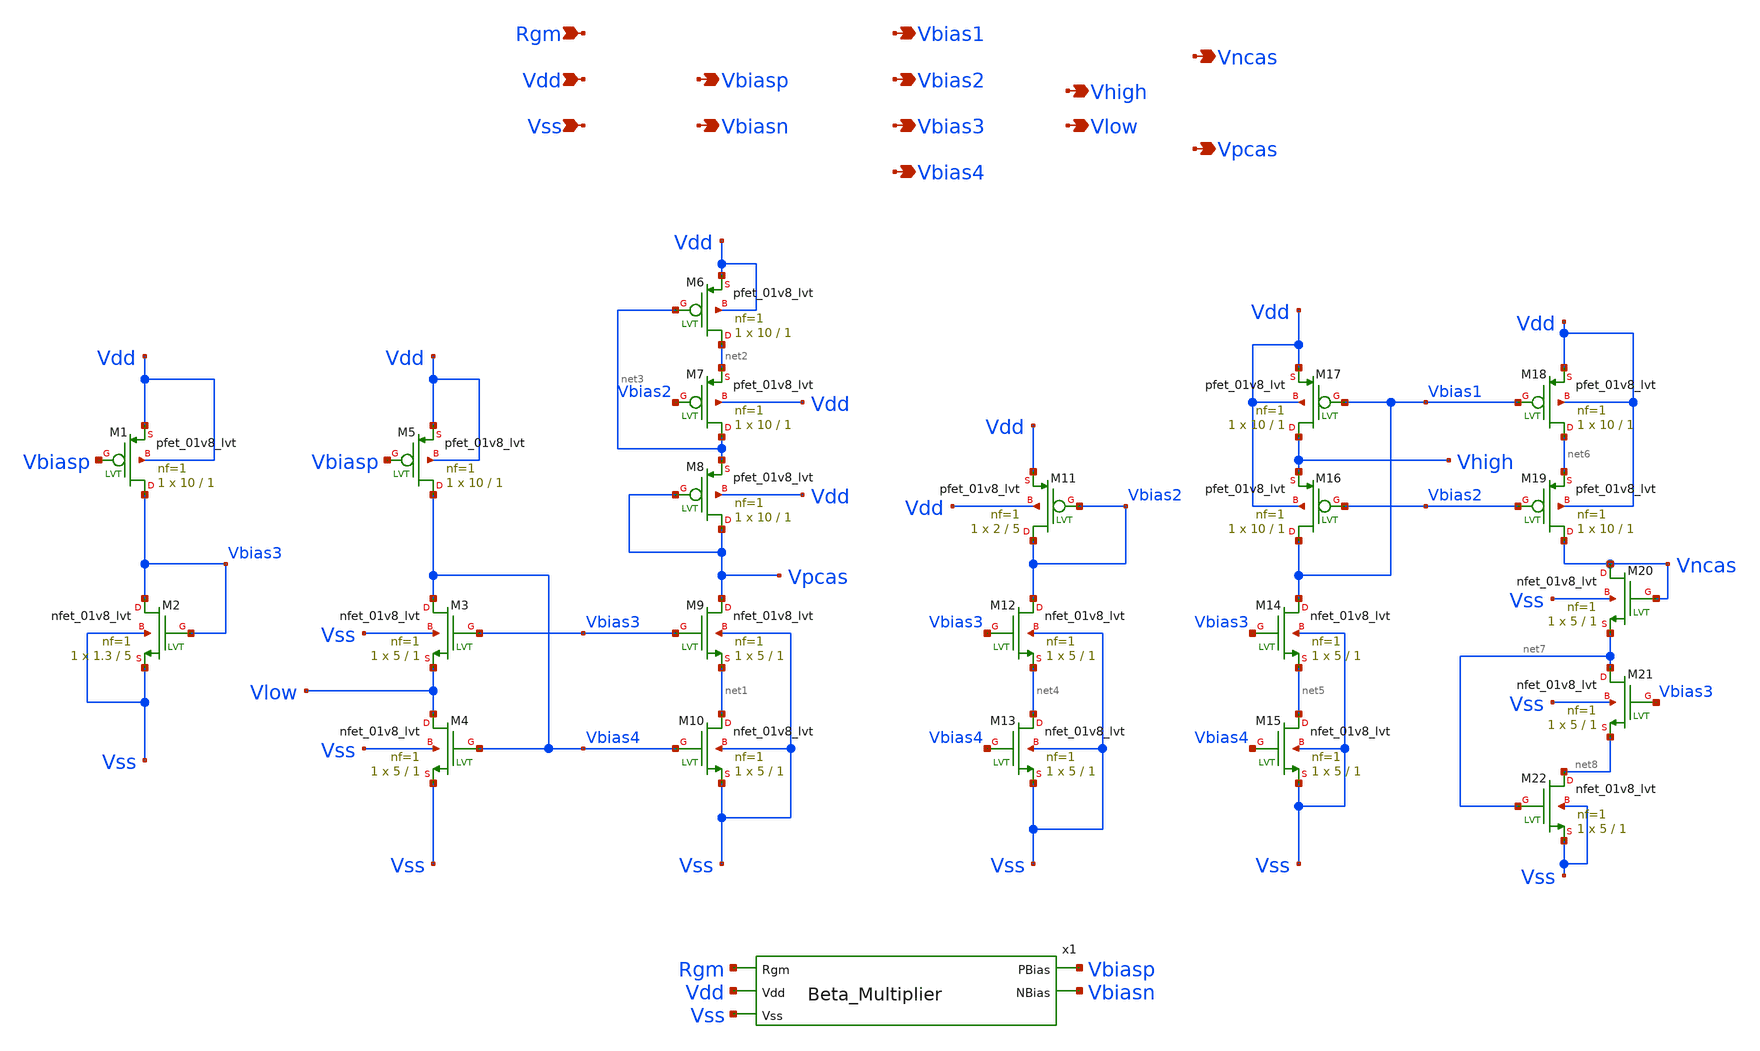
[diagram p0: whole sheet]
** sch_path: src/Opamp_Design/src/Bias_Circuit.sch
**.subckt Bias_Circuit Vdd Vbiasp Vss Vbiasn Vbias1 Vbias2 Vbias3 Vbias4 Vpcas Vlow Vncas Vhigh Rgm
*.ipin Vdd
*.opin Vbiasp
*.ipin Vss
*.opin Vbiasn
*.opin Vbias1
*.opin Vbias2
*.opin Vbias3
*.opin Vbias4
*.opin Vpcas
*.opin Vlow
*.opin Vncas
*.opin Vhigh
*.ipin Rgm
XM1 Vbias3 Vbiasp Vdd Vdd sky130_fd_pr__pfet_01v8_lvt L=1 W=10 nf=1 ad='int((nf+1)/2) * W/nf * 0.29'
+ as='int((nf+2)/2) * W/nf * 0.29' pd='2*int((nf+1)/2) * (W/nf + 0.29)' ps='2*int((nf+2)/2) * (W/nf + 0.29)'
+ nrd='0.29 / W' nrs='0.29 / W' sa=0 sb=0 sd=0 mult=1 m=1
XM2 Vbias3 Vbias3 Vss Vss sky130_fd_pr__nfet_01v8_lvt L=5 W=1.3 nf=1 ad='int((nf+1)/2) * W/nf * 0.29'
+ as='int((nf+2)/2) * W/nf * 0.29' pd='2*int((nf+1)/2) * (W/nf + 0.29)' ps='2*int((nf+2)/2) * (W/nf + 0.29)'
+ nrd='0.29 / W' nrs='0.29 / W' sa=0 sb=0 sd=0 mult=1 m=1
XM3 Vbias4 Vbias3 Vlow Vss sky130_fd_pr__nfet_01v8_lvt L=1 W=5 nf=1 ad='int((nf+1)/2) * W/nf * 0.29'
+ as='int((nf+2)/2) * W/nf * 0.29' pd='2*int((nf+1)/2) * (W/nf + 0.29)' ps='2*int((nf+2)/2) * (W/nf + 0.29)'
+ nrd='0.29 / W' nrs='0.29 / W' sa=0 sb=0 sd=0 mult=1 m=1
XM4 Vlow Vbias4 Vss Vss sky130_fd_pr__nfet_01v8_lvt L=1 W=5 nf=1 ad='int((nf+1)/2) * W/nf * 0.29' as='int((nf+2)/2) * W/nf * 0.29'
+ pd='2*int((nf+1)/2) * (W/nf + 0.29)' ps='2*int((nf+2)/2) * (W/nf + 0.29)' nrd='0.29 / W' nrs='0.29 / W'
+ sa=0 sb=0 sd=0 mult=1 m=1
XM5 Vbias4 Vbiasp Vdd Vdd sky130_fd_pr__pfet_01v8_lvt L=1 W=10 nf=1 ad='int((nf+1)/2) * W/nf * 0.29'
+ as='int((nf+2)/2) * W/nf * 0.29' pd='2*int((nf+1)/2) * (W/nf + 0.29)' ps='2*int((nf+2)/2) * (W/nf + 0.29)'
+ nrd='0.29 / W' nrs='0.29 / W' sa=0 sb=0 sd=0 mult=1 m=1
XM6 net2 net3 Vdd Vdd sky130_fd_pr__pfet_01v8_lvt L=1 W=10 nf=1 ad='int((nf+1)/2) * W/nf * 0.29' as='int((nf+2)/2) * W/nf * 0.29'
+ pd='2*int((nf+1)/2) * (W/nf + 0.29)' ps='2*int((nf+2)/2) * (W/nf + 0.29)' nrd='0.29 / W' nrs='0.29 / W'
+ sa=0 sb=0 sd=0 mult=1 m=1
XM7 net3 Vbias2 net2 Vdd sky130_fd_pr__pfet_01v8_lvt L=1 W=10 nf=1 ad='int((nf+1)/2) * W/nf * 0.29' as='int((nf+2)/2) * W/nf * 0.29'
+ pd='2*int((nf+1)/2) * (W/nf + 0.29)' ps='2*int((nf+2)/2) * (W/nf + 0.29)' nrd='0.29 / W' nrs='0.29 / W'
+ sa=0 sb=0 sd=0 mult=1 m=1
XM8 Vpcas Vpcas net3 Vdd sky130_fd_pr__pfet_01v8_lvt L=1 W=10 nf=1 ad='int((nf+1)/2) * W/nf * 0.29' as='int((nf+2)/2) * W/nf * 0.29'
+ pd='2*int((nf+1)/2) * (W/nf + 0.29)' ps='2*int((nf+2)/2) * (W/nf + 0.29)' nrd='0.29 / W' nrs='0.29 / W'
+ sa=0 sb=0 sd=0 mult=1 m=1
XM9 Vpcas Vbias3 net1 Vss sky130_fd_pr__nfet_01v8_lvt L=1 W=5 nf=1 ad='int((nf+1)/2) * W/nf * 0.29' as='int((nf+2)/2) * W/nf * 0.29'
+ pd='2*int((nf+1)/2) * (W/nf + 0.29)' ps='2*int((nf+2)/2) * (W/nf + 0.29)' nrd='0.29 / W' nrs='0.29 / W'
+ sa=0 sb=0 sd=0 mult=1 m=1
XM10 net1 Vbias4 Vss Vss sky130_fd_pr__nfet_01v8_lvt L=1 W=5 nf=1 ad='int((nf+1)/2) * W/nf * 0.29' as='int((nf+2)/2) * W/nf * 0.29'
+ pd='2*int((nf+1)/2) * (W/nf + 0.29)' ps='2*int((nf+2)/2) * (W/nf + 0.29)' nrd='0.29 / W' nrs='0.29 / W'
+ sa=0 sb=0 sd=0 mult=1 m=1
XM11 Vbias2 Vbias2 Vdd Vdd sky130_fd_pr__pfet_01v8_lvt L=5 W=2 nf=1 ad='int((nf+1)/2) * W/nf * 0.29'
+ as='int((nf+2)/2) * W/nf * 0.29' pd='2*int((nf+1)/2) * (W/nf + 0.29)' ps='2*int((nf+2)/2) * (W/nf + 0.29)'
+ nrd='0.29 / W' nrs='0.29 / W' sa=0 sb=0 sd=0 mult=1 m=1
XM12 Vbias2 Vbias3 net4 Vss sky130_fd_pr__nfet_01v8_lvt L=1 W=5 nf=1 ad='int((nf+1)/2) * W/nf * 0.29'
+ as='int((nf+2)/2) * W/nf * 0.29' pd='2*int((nf+1)/2) * (W/nf + 0.29)' ps='2*int((nf+2)/2) * (W/nf + 0.29)'
+ nrd='0.29 / W' nrs='0.29 / W' sa=0 sb=0 sd=0 mult=1 m=1
XM13 net4 Vbias4 Vss Vss sky130_fd_pr__nfet_01v8_lvt L=1 W=5 nf=1 ad='int((nf+1)/2) * W/nf * 0.29' as='int((nf+2)/2) * W/nf * 0.29'
+ pd='2*int((nf+1)/2) * (W/nf + 0.29)' ps='2*int((nf+2)/2) * (W/nf + 0.29)' nrd='0.29 / W' nrs='0.29 / W'
+ sa=0 sb=0 sd=0 mult=1 m=1
XM14 Vbias1 Vbias3 net5 Vss sky130_fd_pr__nfet_01v8_lvt L=1 W=5 nf=1 ad='int((nf+1)/2) * W/nf * 0.29'
+ as='int((nf+2)/2) * W/nf * 0.29' pd='2*int((nf+1)/2) * (W/nf + 0.29)' ps='2*int((nf+2)/2) * (W/nf + 0.29)'
+ nrd='0.29 / W' nrs='0.29 / W' sa=0 sb=0 sd=0 mult=1 m=1
XM15 net5 Vbias4 Vss Vss sky130_fd_pr__nfet_01v8_lvt L=1 W=5 nf=1 ad='int((nf+1)/2) * W/nf * 0.29' as='int((nf+2)/2) * W/nf * 0.29'
+ pd='2*int((nf+1)/2) * (W/nf + 0.29)' ps='2*int((nf+2)/2) * (W/nf + 0.29)' nrd='0.29 / W' nrs='0.29 / W'
+ sa=0 sb=0 sd=0 mult=1 m=1
XM16 Vbias1 Vbias2 Vhigh Vdd sky130_fd_pr__pfet_01v8_lvt L=1 W=10 nf=1 ad='int((nf+1)/2) * W/nf * 0.29'
+ as='int((nf+2)/2) * W/nf * 0.29' pd='2*int((nf+1)/2) * (W/nf + 0.29)' ps='2*int((nf+2)/2) * (W/nf + 0.29)'
+ nrd='0.29 / W' nrs='0.29 / W' sa=0 sb=0 sd=0 mult=1 m=1
XM17 Vhigh Vbias1 Vdd Vdd sky130_fd_pr__pfet_01v8_lvt L=1 W=10 nf=1 ad='int((nf+1)/2) * W/nf * 0.29'
+ as='int((nf+2)/2) * W/nf * 0.29' pd='2*int((nf+1)/2) * (W/nf + 0.29)' ps='2*int((nf+2)/2) * (W/nf + 0.29)'
+ nrd='0.29 / W' nrs='0.29 / W' sa=0 sb=0 sd=0 mult=1 m=1
XM18 net6 Vbias1 Vdd Vdd sky130_fd_pr__pfet_01v8_lvt L=1 W=10 nf=1 ad='int((nf+1)/2) * W/nf * 0.29' as='int((nf+2)/2) * W/nf * 0.29'
+ pd='2*int((nf+1)/2) * (W/nf + 0.29)' ps='2*int((nf+2)/2) * (W/nf + 0.29)' nrd='0.29 / W' nrs='0.29 / W'
+ sa=0 sb=0 sd=0 mult=1 m=1
XM19 Vncas Vbias2 net6 Vdd sky130_fd_pr__pfet_01v8_lvt L=1 W=10 nf=1 ad='int((nf+1)/2) * W/nf * 0.29'
+ as='int((nf+2)/2) * W/nf * 0.29' pd='2*int((nf+1)/2) * (W/nf + 0.29)' ps='2*int((nf+2)/2) * (W/nf + 0.29)'
+ nrd='0.29 / W' nrs='0.29 / W' sa=0 sb=0 sd=0 mult=1 m=1
XM20 Vncas Vncas net7 Vss sky130_fd_pr__nfet_01v8_lvt L=1 W=5 nf=1 ad='int((nf+1)/2) * W/nf * 0.29' as='int((nf+2)/2) * W/nf * 0.29'
+ pd='2*int((nf+1)/2) * (W/nf + 0.29)' ps='2*int((nf+2)/2) * (W/nf + 0.29)' nrd='0.29 / W' nrs='0.29 / W'
+ sa=0 sb=0 sd=0 mult=1 m=1
XM21 net7 Vbias3 net8 Vss sky130_fd_pr__nfet_01v8_lvt L=1 W=5 nf=1 ad='int((nf+1)/2) * W/nf * 0.29' as='int((nf+2)/2) * W/nf * 0.29'
+ pd='2*int((nf+1)/2) * (W/nf + 0.29)' ps='2*int((nf+2)/2) * (W/nf + 0.29)' nrd='0.29 / W' nrs='0.29 / W'
+ sa=0 sb=0 sd=0 mult=1 m=1
XM22 net8 net7 Vss Vss sky130_fd_pr__nfet_01v8_lvt L=1 W=5 nf=1 ad='int((nf+1)/2) * W/nf * 0.29' as='int((nf+2)/2) * W/nf * 0.29'
+ pd='2*int((nf+1)/2) * (W/nf + 0.29)' ps='2*int((nf+2)/2) * (W/nf + 0.29)' nrd='0.29 / W' nrs='0.29 / W'
+ sa=0 sb=0 sd=0 mult=1 m=1
x1 Rgm Vdd Vss Vbiasp Vbiasn Beta_Multiplier
**.ends

* expanding   symbol:  /foss/designs/FYP/Sky130_Design/Opamp_Design/src/Beta_Multiplier.sym # of
*+ pins=5
** sym_path: src/Opamp_Design/src/Beta_Multiplier.sym
** sch_path: src/Opamp_Design/src/Beta_Multiplier.sch
.subckt Beta_Multiplier Rgm Vdd Vss PBias NBias
*.ipin Vdd
*.opin PBias
*.ipin Vss
*.opin NBias
*.ipin Rgm
XM1 NBias PBias Vdd Vdd sky130_fd_pr__pfet_01v8_lvt L=1 W=10 nf=1 ad='int((nf+1)/2) * W/nf * 0.29' as='int((nf+2)/2) * W/nf * 0.29'
+ pd='2*int((nf+1)/2) * (W/nf + 0.29)' ps='2*int((nf+2)/2) * (W/nf + 0.29)' nrd='0.29 / W' nrs='0.29 / W'
+ sa=0 sb=0 sd=0 mult=1 m=1
XM2 NBias NBias Vss Vss sky130_fd_pr__nfet_01v8_lvt L=1 W=5 nf=1 ad='int((nf+1)/2) * W/nf * 0.29' as='int((nf+2)/2) * W/nf * 0.29'
+ pd='2*int((nf+1)/2) * (W/nf + 0.29)' ps='2*int((nf+2)/2) * (W/nf + 0.29)' nrd='0.29 / W' nrs='0.29 / W'
+ sa=0 sb=0 sd=0 mult=1 m=1
XM3 net1 PBias Vdd Vdd sky130_fd_pr__pfet_01v8_lvt L=1 W=10 nf=1 ad='int((nf+1)/2) * W/nf * 0.29' as='int((nf+2)/2) * W/nf * 0.29'
+ pd='2*int((nf+1)/2) * (W/nf + 0.29)' ps='2*int((nf+2)/2) * (W/nf + 0.29)' nrd='0.29 / W' nrs='0.29 / W'
+ sa=0 sb=0 sd=0 mult=1 m=1
XM4 net1 net1 Rgm Vss sky130_fd_pr__nfet_01v8_lvt L=1 W=20 nf=1 ad='int((nf+1)/2) * W/nf * 0.29' as='int((nf+2)/2) * W/nf * 0.29'
+ pd='2*int((nf+1)/2) * (W/nf + 0.29)' ps='2*int((nf+2)/2) * (W/nf + 0.29)' nrd='0.29 / W' nrs='0.29 / W'
+ sa=0 sb=0 sd=0 mult=1 m=1
XM5 net2 net1 Vss Vss sky130_fd_pr__nfet_01v8_lvt L=1 W=5 nf=1 ad='int((nf+1)/2) * W/nf * 0.29' as='int((nf+2)/2) * W/nf * 0.29'
+ pd='2*int((nf+1)/2) * (W/nf + 0.29)' ps='2*int((nf+2)/2) * (W/nf + 0.29)' nrd='0.29 / W' nrs='0.29 / W'
+ sa=0 sb=0 sd=0 mult=1 m=1
XM6 PBias NBias Vss Vss sky130_fd_pr__nfet_01v8_lvt L=1 W=5 nf=1 ad='int((nf+1)/2) * W/nf * 0.29' as='int((nf+2)/2) * W/nf * 0.29'
+ pd='2*int((nf+1)/2) * (W/nf + 0.29)' ps='2*int((nf+2)/2) * (W/nf + 0.29)' nrd='0.29 / W' nrs='0.29 / W'
+ sa=0 sb=0 sd=0 mult=1 m=1
XM7 PBias net2 Vdd Vdd sky130_fd_pr__pfet_01v8_lvt L=1 W=10 nf=1 ad='int((nf+1)/2) * W/nf * 0.29' as='int((nf+2)/2) * W/nf * 0.29'
+ pd='2*int((nf+1)/2) * (W/nf + 0.29)' ps='2*int((nf+2)/2) * (W/nf + 0.29)' nrd='0.29 / W' nrs='0.29 / W'
+ sa=0 sb=0 sd=0 mult=1 m=1
XM8 net2 net2 Vdd Vdd sky130_fd_pr__pfet_01v8_lvt L=1 W=10 nf=1 ad='int((nf+1)/2) * W/nf * 0.29' as='int((nf+2)/2) * W/nf * 0.29'
+ pd='2*int((nf+1)/2) * (W/nf + 0.29)' ps='2*int((nf+2)/2) * (W/nf + 0.29)' nrd='0.29 / W' nrs='0.29 / W'
+ sa=0 sb=0 sd=0 mult=1 m=1
XM9 PBias net3 NBias Vss sky130_fd_pr__nfet_01v8_lvt L=1 W=2 nf=1 ad='int((nf+1)/2) * W/nf * 0.29' as='int((nf+2)/2) * W/nf * 0.29'
+ pd='2*int((nf+1)/2) * (W/nf + 0.29)' ps='2*int((nf+2)/2) * (W/nf + 0.29)' nrd='0.29 / W' nrs='0.29 / W'
+ sa=0 sb=0 sd=0 mult=1 m=1
XM10 net3 NBias Vss Vss sky130_fd_pr__nfet_01v8_lvt L=1 W=5 nf=1 ad='int((nf+1)/2) * W/nf * 0.29' as='int((nf+2)/2) * W/nf * 0.29'
+ pd='2*int((nf+1)/2) * (W/nf + 0.29)' ps='2*int((nf+2)/2) * (W/nf + 0.29)' nrd='0.29 / W' nrs='0.29 / W'
+ sa=0 sb=0 sd=0 mult=1 m=1
XM11 net3 net3 Vdd Vdd sky130_fd_pr__pfet_01v8_lvt L=10 W=1 nf=1 ad='int((nf+1)/2) * W/nf * 0.29' as='int((nf+2)/2) * W/nf * 0.29'
+ pd='2*int((nf+1)/2) * (W/nf + 0.29)' ps='2*int((nf+2)/2) * (W/nf + 0.29)' nrd='0.29 / W' nrs='0.29 / W'
+ sa=0 sb=0 sd=0 mult=1 m=1
.ends

.end
